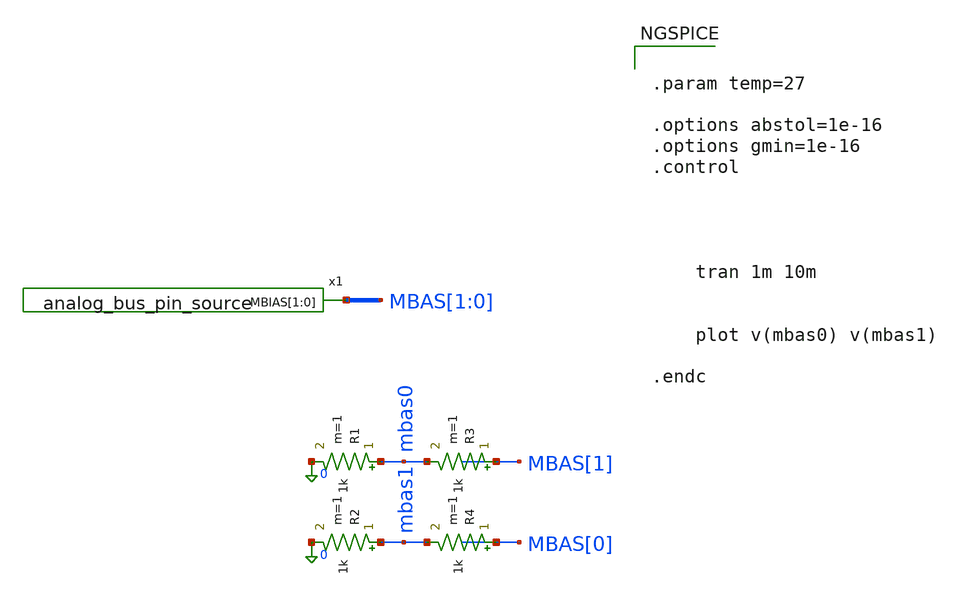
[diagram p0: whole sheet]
** sch_path: test_bench/analog_bus_pin_tb.sch
**.subckt analog_bus_pin_tb
x1 MBAS[1] MBAS[0] analog_bus_pin_source
R1 mbas0 0 1k m=1
R2 mbas1 0 1k m=1
R3 MBAS[1] mbas0 1k m=1
R4 MBAS[0] mbas1 1k m=1
**** begin user architecture code


.param temp=27

.options abstol=1e-16
.options gmin=1e-16
.control




    tran 1m 10m


    plot v(mbas0) v(mbas1)

.endc


**** end user architecture code
**.ends

* expanding   symbol:  test_bench/analog_bus_pin_source.sym # of pins=1
** sym_path: test_bench/analog_bus_pin_source.sym
** sch_path: test_bench/analog_bus_pin_source.sch
.subckt analog_bus_pin_source MBIAS[1] MBIAS[0]
*.opin MBIAS[1],MBIAS[0]
V1 MBIAS[0] 0 3
V2 MBIAS[1] 0 1
.ends

.end
